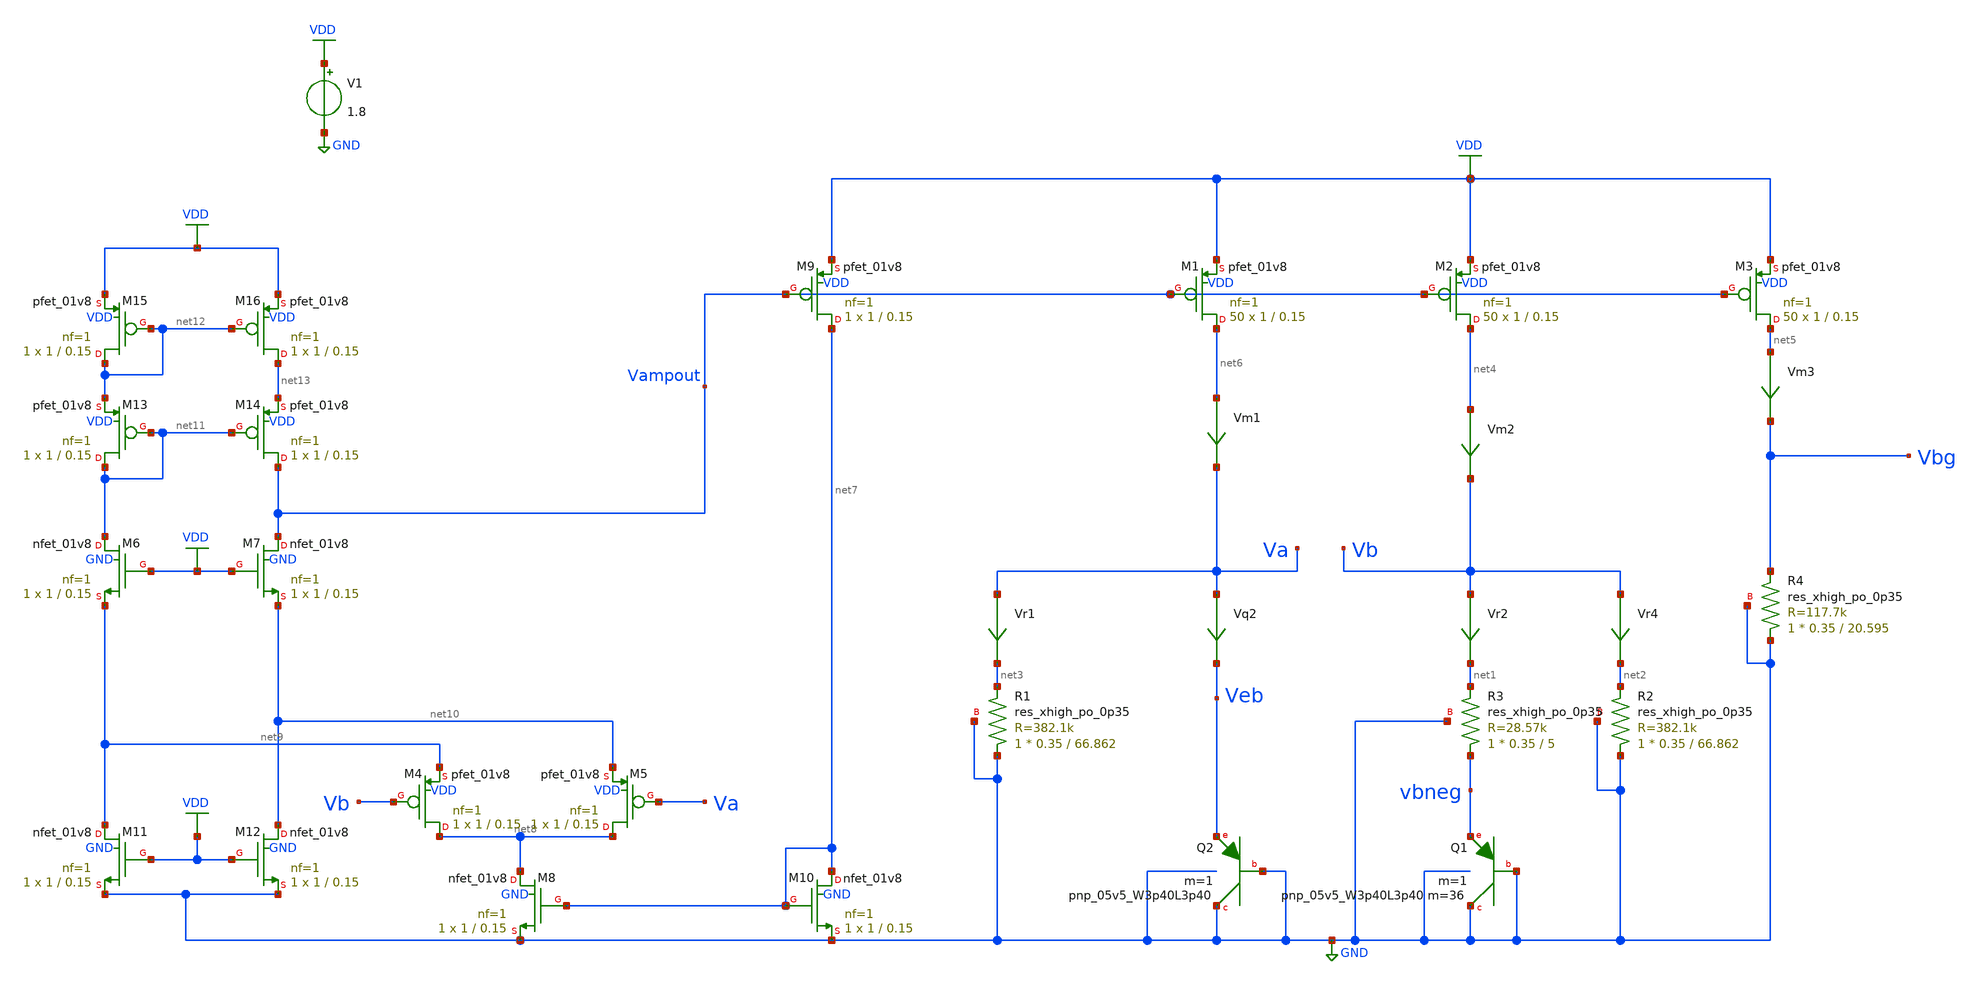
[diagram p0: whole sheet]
** sch_path: schematics/tsmc_bandgap_w_amp.sch
**.subckt tsmc_bandgap_w_amp
XQ2 GND GND Veb sky130_fd_pr__pnp_05v5_W3p40L3p40 m=1
V1 VDD GND 1.8
Vr4 Vb net2 0
.save i(vr4)
Vr2 Vb net1 0
.save i(vr2)
Vm1 net6 Va 0
.save i(vm1)
Vm2 net4 Vb 0
.save i(vm2)
Vm3 net5 Vbg 0
.save i(vm3)
Vr1 Va net3 0
.save i(vr1)
Vq2 Va Veb 0
.save i(vq2)
XQ1 GND GND vbneg sky130_fd_pr__pnp_05v5_W3p40L3p40 m=36 m=1
XR1 GND net3 GND sky130_fd_pr__res_xhigh_po_0p35 L=66.862 mult=1 m=1
XR2 GND net2 GND sky130_fd_pr__res_xhigh_po_0p35 L=66.862 mult=1 m=1
XR3 vbneg net1 GND sky130_fd_pr__res_xhigh_po_0p35 L=5 mult=1 m=1
XR4 GND Vbg GND sky130_fd_pr__res_xhigh_po_0p35 L=20.595 mult=1 m=1
XM1 net6 Vampout VDD VDD sky130_fd_pr__pfet_01v8 L=0.15 W=1 nf=1 ad='int((nf+1)/2) * W/nf * 0.29' as='int((nf+2)/2) * W/nf * 0.29'
+ pd='2*int((nf+1)/2) * (W/nf + 0.29)' ps='2*int((nf+2)/2) * (W/nf + 0.29)' nrd='0.29 / W' nrs='0.29 / W'
+ sa=0 sb=0 sd=0 mult=50 m=50
XM2 net4 Vampout VDD VDD sky130_fd_pr__pfet_01v8 L=0.15 W=1 nf=1 ad='int((nf+1)/2) * W/nf * 0.29' as='int((nf+2)/2) * W/nf * 0.29'
+ pd='2*int((nf+1)/2) * (W/nf + 0.29)' ps='2*int((nf+2)/2) * (W/nf + 0.29)' nrd='0.29 / W' nrs='0.29 / W'
+ sa=0 sb=0 sd=0 mult=50 m=50
XM3 net5 Vampout VDD VDD sky130_fd_pr__pfet_01v8 L=0.15 W=1 nf=1 ad='int((nf+1)/2) * W/nf * 0.29' as='int((nf+2)/2) * W/nf * 0.29'
+ pd='2*int((nf+1)/2) * (W/nf + 0.29)' ps='2*int((nf+2)/2) * (W/nf + 0.29)' nrd='0.29 / W' nrs='0.29 / W'
+ sa=0 sb=0 sd=0 mult=50 m=50
XM4 net8 Vb net9 VDD sky130_fd_pr__pfet_01v8 L=0.15 W=1 nf=1 ad='int((nf+1)/2) * W/nf * 0.29' as='int((nf+2)/2) * W/nf * 0.29'
+ pd='2*int((nf+1)/2) * (W/nf + 0.29)' ps='2*int((nf+2)/2) * (W/nf + 0.29)' nrd='0.29 / W' nrs='0.29 / W'
+ sa=0 sb=0 sd=0 mult=1 m=1
XM8 net8 net7 GND GND sky130_fd_pr__nfet_01v8 L=0.15 W=1 nf=1 ad='int((nf+1)/2) * W/nf * 0.29' as='int((nf+2)/2) * W/nf * 0.29'
+ pd='2*int((nf+1)/2) * (W/nf + 0.29)' ps='2*int((nf+2)/2) * (W/nf + 0.29)' nrd='0.29 / W' nrs='0.29 / W'
+ sa=0 sb=0 sd=0 mult=1 m=1
XM5 net8 Va net10 VDD sky130_fd_pr__pfet_01v8 L=0.15 W=1 nf=1 ad='int((nf+1)/2) * W/nf * 0.29' as='int((nf+2)/2) * W/nf * 0.29'
+ pd='2*int((nf+1)/2) * (W/nf + 0.29)' ps='2*int((nf+2)/2) * (W/nf + 0.29)' nrd='0.29 / W' nrs='0.29 / W'
+ sa=0 sb=0 sd=0 mult=1 m=1
XM9 net7 Vampout VDD VDD sky130_fd_pr__pfet_01v8 L=0.15 W=1 nf=1 ad='int((nf+1)/2) * W/nf * 0.29' as='int((nf+2)/2) * W/nf * 0.29'
+ pd='2*int((nf+1)/2) * (W/nf + 0.29)' ps='2*int((nf+2)/2) * (W/nf + 0.29)' nrd='0.29 / W' nrs='0.29 / W'
+ sa=0 sb=0 sd=0 mult=1 m=1
XM10 net7 net7 GND GND sky130_fd_pr__nfet_01v8 L=0.15 W=1 nf=1 ad='int((nf+1)/2) * W/nf * 0.29' as='int((nf+2)/2) * W/nf * 0.29'
+ pd='2*int((nf+1)/2) * (W/nf + 0.29)' ps='2*int((nf+2)/2) * (W/nf + 0.29)' nrd='0.29 / W' nrs='0.29 / W'
+ sa=0 sb=0 sd=0 mult=1 m=1
XM11 net9 VDD GND GND sky130_fd_pr__nfet_01v8 L=0.15 W=1 nf=1 ad='int((nf+1)/2) * W/nf * 0.29' as='int((nf+2)/2) * W/nf * 0.29'
+ pd='2*int((nf+1)/2) * (W/nf + 0.29)' ps='2*int((nf+2)/2) * (W/nf + 0.29)' nrd='0.29 / W' nrs='0.29 / W'
+ sa=0 sb=0 sd=0 mult=1 m=1
XM12 net10 VDD GND GND sky130_fd_pr__nfet_01v8 L=0.15 W=1 nf=1 ad='int((nf+1)/2) * W/nf * 0.29' as='int((nf+2)/2) * W/nf * 0.29'
+ pd='2*int((nf+1)/2) * (W/nf + 0.29)' ps='2*int((nf+2)/2) * (W/nf + 0.29)' nrd='0.29 / W' nrs='0.29 / W'
+ sa=0 sb=0 sd=0 mult=1 m=1
XM6 net11 VDD net9 GND sky130_fd_pr__nfet_01v8 L=0.15 W=1 nf=1 ad='int((nf+1)/2) * W/nf * 0.29' as='int((nf+2)/2) * W/nf * 0.29'
+ pd='2*int((nf+1)/2) * (W/nf + 0.29)' ps='2*int((nf+2)/2) * (W/nf + 0.29)' nrd='0.29 / W' nrs='0.29 / W'
+ sa=0 sb=0 sd=0 mult=1 m=1
XM7 Vampout VDD net10 GND sky130_fd_pr__nfet_01v8 L=0.15 W=1 nf=1 ad='int((nf+1)/2) * W/nf * 0.29' as='int((nf+2)/2) * W/nf * 0.29'
+ pd='2*int((nf+1)/2) * (W/nf + 0.29)' ps='2*int((nf+2)/2) * (W/nf + 0.29)' nrd='0.29 / W' nrs='0.29 / W'
+ sa=0 sb=0 sd=0 mult=1 m=1
XM13 net11 net11 net12 VDD sky130_fd_pr__pfet_01v8 L=0.15 W=1 nf=1 ad='int((nf+1)/2) * W/nf * 0.29' as='int((nf+2)/2) * W/nf * 0.29'
+ pd='2*int((nf+1)/2) * (W/nf + 0.29)' ps='2*int((nf+2)/2) * (W/nf + 0.29)' nrd='0.29 / W' nrs='0.29 / W'
+ sa=0 sb=0 sd=0 mult=1 m=1
XM14 Vampout net11 net13 VDD sky130_fd_pr__pfet_01v8 L=0.15 W=1 nf=1 ad='int((nf+1)/2) * W/nf * 0.29'
+ as='int((nf+2)/2) * W/nf * 0.29' pd='2*int((nf+1)/2) * (W/nf + 0.29)' ps='2*int((nf+2)/2) * (W/nf + 0.29)'
+ nrd='0.29 / W' nrs='0.29 / W' sa=0 sb=0 sd=0 mult=1 m=1
XM15 net12 net12 VDD VDD sky130_fd_pr__pfet_01v8 L=0.15 W=1 nf=1 ad='int((nf+1)/2) * W/nf * 0.29' as='int((nf+2)/2) * W/nf * 0.29'
+ pd='2*int((nf+1)/2) * (W/nf + 0.29)' ps='2*int((nf+2)/2) * (W/nf + 0.29)' nrd='0.29 / W' nrs='0.29 / W'
+ sa=0 sb=0 sd=0 mult=1 m=1
XM16 net13 net12 VDD VDD sky130_fd_pr__pfet_01v8 L=0.15 W=1 nf=1 ad='int((nf+1)/2) * W/nf * 0.29' as='int((nf+2)/2) * W/nf * 0.29'
+ pd='2*int((nf+1)/2) * (W/nf + 0.29)' ps='2*int((nf+2)/2) * (W/nf + 0.29)' nrd='0.29 / W' nrs='0.29 / W'
+ sa=0 sb=0 sd=0 mult=1 m=1
**** begin user architecture code

.include $::SKYWATER_MODELS/cells/nfet_01v8/sky130_fd_pr__nfet_01v8__tt.corner.spice
.include $::SKYWATER_MODELS/cells/nfet_01v8_lvt/sky130_fd_pr__nfet_01v8_lvt__tt.corner.spice
.include $::SKYWATER_MODELS/cells/pfet_01v8/sky130_fd_pr__pfet_01v8__tt.corner.spice
.include $::SKYWATER_MODELS/cells/nfet_03v3_nvt/sky130_fd_pr__nfet_03v3_nvt__tt.corner.spice
.include $::SKYWATER_MODELS/cells/nfet_05v0_nvt/sky130_fd_pr__nfet_05v0_nvt__tt.corner.spice
.include $::SKYWATER_MODELS/cells/esd_nfet_01v8/sky130_fd_pr__esd_nfet_01v8__tt.corner.spice
.include $::SKYWATER_MODELS/cells/pfet_01v8_lvt/sky130_fd_pr__pfet_01v8_lvt__tt.corner.spice
.include $::SKYWATER_MODELS/cells/pfet_01v8_hvt/sky130_fd_pr__pfet_01v8_hvt__tt.corner.spice
.include $::SKYWATER_MODELS/cells/esd_pfet_g5v0d10v5/sky130_fd_pr__esd_pfet_g5v0d10v5__tt.corner.spice
.include $::SKYWATER_MODELS/cells/pfet_g5v0d10v5/sky130_fd_pr__pfet_g5v0d10v5__tt.corner.spice
.include $::SKYWATER_MODELS/cells/pfet_g5v0d16v0/sky130_fd_pr__pfet_g5v0d16v0__tt.corner.spice
.include $::SKYWATER_MODELS/cells/nfet_g5v0d10v5/sky130_fd_pr__nfet_g5v0d10v5__tt.corner.spice
.include $::SKYWATER_MODELS/cells/nfet_g5v0d16v0/sky130_fd_pr__nfet_g5v0d16v0__tt_discrete.corner.spice
.include $::SKYWATER_MODELS/cells/esd_nfet_g5v0d10v5/sky130_fd_pr__esd_nfet_g5v0d10v5__tt.corner.spice
.include $::SKYWATER_MODELS/models/corners/tt/nonfet.spice
* Mismatch parameters
.include $::SKYWATER_MODELS/cells/nfet_01v8/sky130_fd_pr__nfet_01v8__mismatch.corner.spice
.include $::SKYWATER_MODELS/cells/pfet_01v8/sky130_fd_pr__pfet_01v8__mismatch.corner.spice
.include $::SKYWATER_MODELS/cells/nfet_01v8_lvt/sky130_fd_pr__nfet_01v8_lvt__mismatch.corner.spice
.include $::SKYWATER_MODELS/cells/pfet_01v8_lvt/sky130_fd_pr__pfet_01v8_lvt__mismatch.corner.spice
.include $::SKYWATER_MODELS/cells/pfet_01v8_hvt/sky130_fd_pr__pfet_01v8_hvt__mismatch.corner.spice
.include $::SKYWATER_MODELS/cells/nfet_g5v0d10v5/sky130_fd_pr__nfet_g5v0d10v5__mismatch.corner.spice
.include $::SKYWATER_MODELS/cells/pfet_g5v0d10v5/sky130_fd_pr__pfet_g5v0d10v5__mismatch.corner.spice
.include $::SKYWATER_MODELS/cells/nfet_05v0_nvt/sky130_fd_pr__nfet_05v0_nvt__mismatch.corner.spice
.include $::SKYWATER_MODELS/cells/nfet_03v3_nvt/sky130_fd_pr__nfet_03v3_nvt__mismatch.corner.spice
* Resistor$::SKYWATER_MODELS/Capacitor
.include $::SKYWATER_MODELS/models/r+c/res_typical__cap_typical.spice
.include $::SKYWATER_MODELS/models/r+c/res_typical__cap_typical__lin.spice
* Special cells
.include $::SKYWATER_MODELS/models/corners/tt/specialized_cells.spice
* All models
.include $::SKYWATER_MODELS/models/all.spice
.include $::SKYWATER_MODELS/cells/pnp_05v5/sky130_fd_pr__pnp_05v5_W3p40L3p40.model.spice
* Corner
.include $::SKYWATER_MODELS/models/corners/tt/rf.spice


* this experimental option enables mos model bin
* selection based on W/NF instead of W
.option wnflag=1
.option savecurrents
.option warn=1
.control
save all
dc TEMP  -20 125 1
plot Vbg
plot deriv(Vbg)
write tsmc_bandgap_temp.raw
op
write tsmc_bandgap_op.raw
print vbg
print (vb - vbneg)
*dc TEMP -40 125 1 R1 57141.79k 6800k 100k
*let start_r = 5756.397788k
*let end_r = 6800k
*let incr_r = 100k
*let r_act = start_r
*while r_act <= end_r
*  alter r2 r_act
*  alter r1 r_act
*  dc temp -40 125 15
*  write dc-sweep.out Vbg deriv(Vbg)
*  set apendwrite
*  let r_act = r_act + incr_r
*end
*plot dc1.vbg dc1.deriv(vbg)
*plot Vbg
*plot deriv(Vbg)
.endc


**** end user architecture code
**.ends
.GLOBAL GND
.GLOBAL VDD
.end
